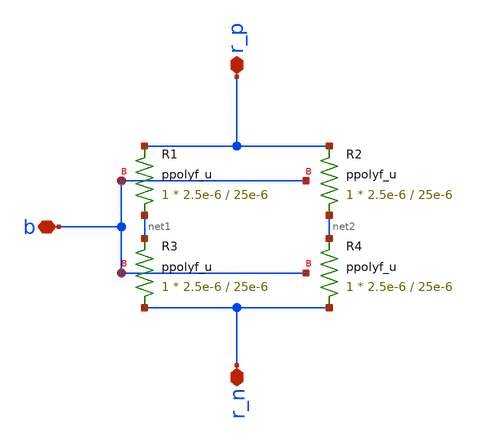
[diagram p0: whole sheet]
** sch_path: designs/libs/core_analog/vref/vref_R1.sch
**.subckt vref_R1 r_p r_n b
*.iopin r_p
*.iopin r_n
*.iopin b
XR1 net1 r_p b ppolyf_u r_width=2.5e-6 r_length=25e-6 m=1
XR2 net2 r_p b ppolyf_u r_width=2.5e-6 r_length=25e-6 m=1
XR3 r_n net1 b ppolyf_u r_width=2.5e-6 r_length=25e-6 m=1
XR4 r_n net2 b ppolyf_u r_width=2.5e-6 r_length=25e-6 m=1
**.ends
.end
